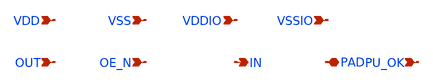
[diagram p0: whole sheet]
** sch_path: sch/pads/ihp130/sdr_bidir_pad.sch
**.subckt sdr_bidir_pad OUT OE_N IN PAD PU_OK VDD VSS VDDIO VSSIO
*.ipin OUT
*.ipin OE_N
*.opin IN
*.iopin PAD
*.ipin PU_OK
*.ipin VDD
*.ipin VSS
*.ipin VDDIO
*.ipin VSSIO
**** begin user architecture code


* GENERATED by generator/emit_pads.py -- DO NOT EDIT BY HAND
* backend: ihp130   pdk: ihp-sg13g2
* topology: specs/pads/topology.yaml v1 -- ONE shared schematic, only device names change
* STATUS: topology_template_only
* license: Apache-2.0 (IHP PDK Authors)
* SIZE UNITS: topology params are metres; HV/LV subckts take w/l in metres (u suffix accepted)
* ESD NOTE: fixed-geometry 2 kV ESD subckts; ESD_AREA_* params are NOT applied
*
* NOT SIMULATABLE. This is a TOPOLOGY TEMPLATE:
*   - every W / L / NF / R / area is an unresolved parameter
*     (see required_params.json). ngspice rejects them until filled.
*   - PAD_OE_CTRL is a generated transistor-level block (IO gates plus
*     an optional core-to-IO level shifter); its devices reuse the
*     pre-driver sizing placeholders and are not optimized.
*   - diode orientation, bulk ties and the series-R third terminal must
*     be confirmed at schematic review; they are NOT signed off here.
*   - L_R_SERIES is the on-chip resistor LENGTH. The target
*     resistance in ohm is a board-level SI input, not a pad param;
*     converting target R to L needs a per-PDK sheet resistance.
*
* Device-instantiation syntax is per backend (nf vs ng, m vs mr,
* r_length/r_width vs w/l, 2-terminal diode model vs 3-terminal ESD
* subckt). It lives in specs/pads/devices/<backend>.yaml; the block
* topology below stays shared.
*
* Expected includes (NOT bundled; integrator supplies models.spice):
*   libs.tech/ngspice/models/cornerMOShv.lib; cornerMOSlv.lib; cornerRES.lib; sg13g2_esd.lib
*   none (device models only)
*
* Shared signal chain (docs/ARCHITECTURE.md section 5):
*   OUT/OE_N --[level shift if VDD != VDDIO]--> pre-driver --> tri-state
*   --> series R --> PAD --> ESD (to VDDIO / VSSIO + power clamp)
*   PAD --> CMOS/Schmitt RX --> [level shift back] --> IN
*   power-up Hi-Z until VDD and VDDIO are both present (PU_OK)

X_INV_P Y A VDDIO VDDIO sg13_hv_pmos w=W_P_PDRV l=L_PDRV ng=NF_DEVICE m=M_DEVICE
X_INV_N Y A VSSIO VSSIO sg13_hv_nmos w=W_N_PDRV l=L_PDRV ng=NF_DEVICE m=M_DEVICE
X_NAND_P1 Y A VDDIO VDDIO sg13_hv_pmos w=W_P_PDRV l=L_PDRV ng=NF_DEVICE m=M_DEVICE
X_NAND_P2 Y B VDDIO VDDIO sg13_hv_pmos w=W_P_PDRV l=L_PDRV ng=NF_DEVICE m=M_DEVICE
X_NAND_N1 Y A nand_mid VSSIO sg13_hv_nmos w=W_N_PDRV l=L_PDRV ng=NF_DEVICE m=M_DEVICE
X_NAND_N2 nand_mid B VSSIO VSSIO sg13_hv_nmos w=W_N_PDRV l=L_PDRV ng=NF_DEVICE m=M_DEVICE
X_NOR_P1 Y A nor_mid VDDIO sg13_hv_pmos w=W_P_PDRV l=L_PDRV ng=NF_DEVICE m=M_DEVICE
X_NOR_P2 nor_mid B VDDIO VDDIO sg13_hv_pmos w=W_P_PDRV l=L_PDRV ng=NF_DEVICE m=M_DEVICE
X_NOR_N1 Y A VSSIO VSSIO sg13_hv_nmos w=W_N_PDRV l=L_PDRV ng=NF_DEVICE m=M_DEVICE
X_NOR_N2 Y B VSSIO VSSIO sg13_hv_nmos w=W_N_PDRV l=L_PDRV ng=NF_DEVICE m=M_DEVICE
X_LS_INV_P INB IN VDD VDD sg13_lv_pmos w=W_P_PDRV l=L_PDRV ng=NF_DEVICE m=M_DEVICE
X_LS_INV_N INB IN VSS VSS sg13_lv_nmos w=W_N_PDRV l=L_PDRV ng=NF_DEVICE m=M_DEVICE
X_LS_N1 OUTB IN VSSIO VSSIO sg13_hv_nmos w=W_N_PDRV*16 l=L_PDRV ng=NF_DEVICE m=M_DEVICE
X_LS_N2 OUT INB VSSIO VSSIO sg13_hv_nmos w=W_N_PDRV*16 l=L_PDRV ng=NF_DEVICE m=M_DEVICE
X_LS_P1 OUTB OUT VDDIO VDDIO sg13_hv_pmos w=W_P_PDRV l=L_PDRV ng=NF_DEVICE m=M_DEVICE
X_LS_P2 OUT OUTB VDDIO VDDIO sg13_hv_pmos w=W_P_PDRV l=L_PDRV ng=NF_DEVICE m=M_DEVICE
X_LS OUT OUT_I OUTB_I VDD VSS VDDIO VSSIO LS_C2I
* OE_N and PU_OK are IO-domain control inputs in this macro
X_INV_OE OE_N OENB VDDIO VSSIO INV_IO
X_NAND PU_OK OENB EN_N VDDIO VSSIO NAND2_IO
X_NOR_GN EN_N OUT_I N_GN VDDIO VSSIO NOR2_IO
X_NOR_GP EN_N OUTB_I NGPB VDDIO VSSIO NOR2_IO
X_INV_NGP NGPB N_GP VDDIO VSSIO INV_IO


* --- OE / power-up gating: real transistor-level block (see header) ---
X_OE_CTRL n_gp n_gn OUT OE_N PU_OK VDD VSS VDDIO VSSIO PAD_OE_CTRL

* --- pre-driver chain (even stage count preserves polarity) ---
X_PDRV_P_GP1 n_gp_s1 n_gp VDDIO VDDIO sg13_hv_pmos w=W_P_PDRV l=L_PDRV ng=NF_DEVICE m=M_DEVICE
X_PDRV_N_GP1 n_gp_s1 n_gp VSSIO VSSIO sg13_hv_nmos w=W_N_PDRV l=L_PDRV ng=NF_DEVICE m=M_DEVICE
X_PDRV_P_GP2 n_gp_drv n_gp_s1 VDDIO VDDIO sg13_hv_pmos w=W_P_PDRV l=L_PDRV ng=NF_DEVICE m=M_DEVICE
X_PDRV_N_GP2 n_gp_drv n_gp_s1 VSSIO VSSIO sg13_hv_nmos w=W_N_PDRV l=L_PDRV ng=NF_DEVICE m=M_DEVICE
X_PDRV_P_GN1 n_gn_s1 n_gn VDDIO VDDIO sg13_hv_pmos w=W_P_PDRV l=L_PDRV ng=NF_DEVICE m=M_DEVICE
X_PDRV_N_GN1 n_gn_s1 n_gn VSSIO VSSIO sg13_hv_nmos w=W_N_PDRV l=L_PDRV ng=NF_DEVICE m=M_DEVICE
X_PDRV_P_GN2 n_gn_drv n_gn_s1 VDDIO VDDIO sg13_hv_pmos w=W_P_PDRV l=L_PDRV ng=NF_DEVICE m=M_DEVICE
X_PDRV_N_GN2 n_gn_drv n_gn_s1 VSSIO VSSIO sg13_hv_nmos w=W_N_PDRV l=L_PDRV ng=NF_DEVICE m=M_DEVICE

* --- tri-state output (PMOS to VDDIO, NMOS to VSSIO) ---
X_OUT_P n_pre n_gp_drv VDDIO VDDIO sg13_hv_pmos w=W_P_OUT l=L_P_OUT ng=NF_P_OUT m=M_DEVICE
X_OUT_N n_pre n_gn_drv VSSIO VSSIO sg13_hv_nmos w=W_N_OUT l=L_N_OUT ng=NF_N_OUT m=M_DEVICE

* --- on-chip series damping resistor (may instead live on the board) ---
X_RSER n_pre PAD VSSIO rppd w=W_R_SERIES l=L_R_SERIES

* --- ESD: primary diodes + VDDIO-to-VSSIO clamp ---
X_ESD_UP VDDIO PAD VSSIO diodevdd_2kv
X_ESD_DN VDDIO PAD VSSIO diodevss_2kv
X_CLAMP VDDIO VSSIO VSSIO diodevdd_2kv

* --- SDR receiver: thick-oxide CMOS inverter (Schmitt optional) ---
X_RX_N IN PAD VSSIO VSSIO sg13_hv_nmos w=W_RX_N l=L_PDRV ng=NF_DEVICE m=M_DEVICE
X_RX_P IN PAD VDDIO VDDIO sg13_hv_pmos w=W_RX_P l=L_PDRV ng=NF_DEVICE m=M_DEVICE
* RX_HYST unresolved; do NOT assume the input threshold equals VDDIO/2.

* --- IO -> core level shifter for IN: topology TBD (not a drawn netlist) ---

* --- guard ring surrounds output stage and ESD (layout only) ---
* GUARD_RING_WIDTH / GUARD_RING_SPACING unresolved; not drawn here.


**** end user architecture code
**.ends
.end
